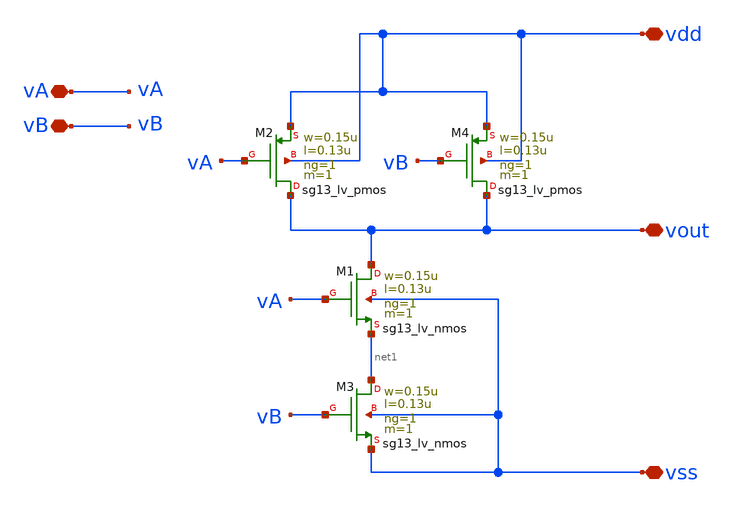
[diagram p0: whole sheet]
** sch_path: design/blocks/nandgate/nandgate.sch
**.subckt nandgate vout vA vB vdd vss
*.iopin vout
*.iopin vA
*.iopin vB
*.iopin vdd
*.iopin vss
XM1 vout vA net1 vss sg13_lv_nmos w=0.15u l=0.13u ng=1 m=1 mm_ok=1
XM2 vout vA vdd vdd sg13_lv_pmos w=0.15u l=0.13u ng=1 m=1 mm_ok=1
XM3 net1 vB vss vss sg13_lv_nmos w=0.15u l=0.13u ng=1 m=1 mm_ok=1
XM4 vout vB vdd vdd sg13_lv_pmos w=0.15u l=0.13u ng=1 m=1 mm_ok=1
**.ends
.end
